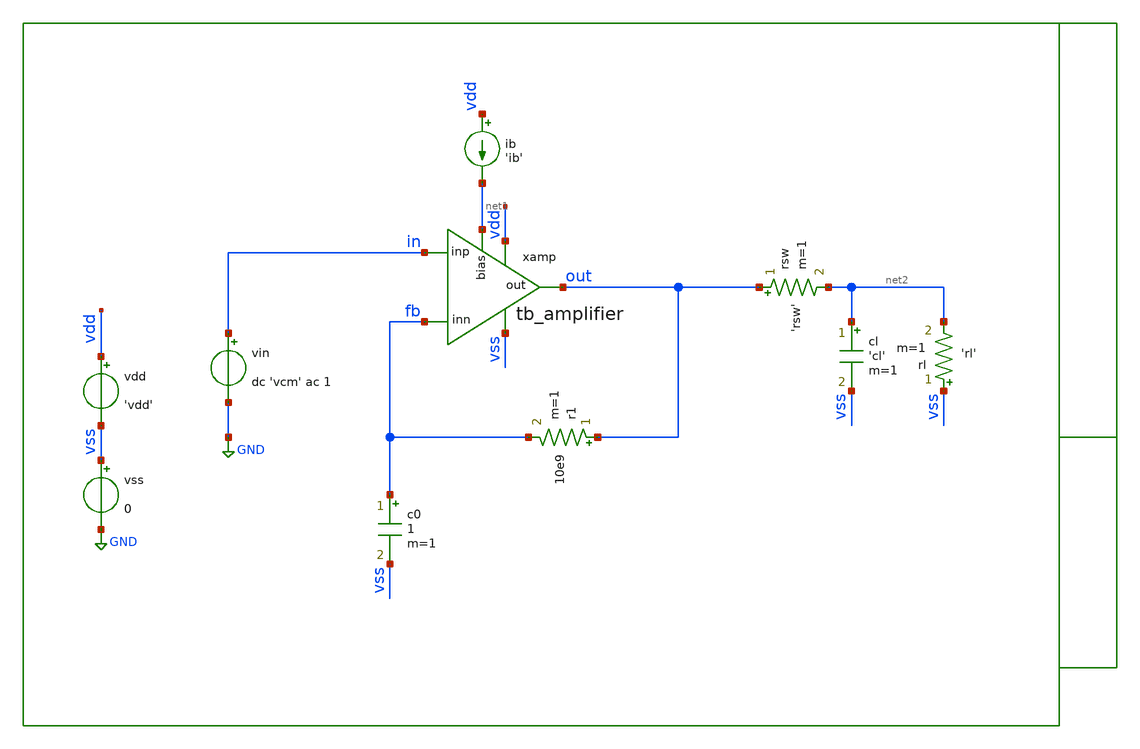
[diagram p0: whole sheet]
** sch_path: xschem/tb/testbuffer/tb_amplifier/no_tb_amplifier.sch
**.subckt no_tb_amplifier
vin in GND dc 'vcm' ac 1
c0 fb vss 1 m=1
r1 out fb 10e9 m=1
ib vdd net1 'ib'
xamp vdd out in fb vss net1 tb_amplifier
vdd vdd vss 'vdd'
vss vss GND 0
cl net2 vss 'cl' m=1
rl vss net2 'rl' m=1
rsw out net2 'rsw' m=1
**** begin user architecture code

* Control

.param vdd=3.3
.param vcm='vdd/2'
.param ib=5u
.param cl=1p
.param rl=10e6
.param rsw=1

.control
save all
noise v(out,vss) vin dec 10 0.1 1e6 1
print inoise_total
print onoise_total
setplot noise1
gnuplot p1 inoise_spectrum
gnuplot p2 onoise_spectrum
set wr_singlescale
set wr_vecnames
wrdata data.csv onoise_spectrum inoise_spectrum
.endc


 * Model Corners

.include $::CORNERS/ngspice/tt.spice
*.include $::CORNERS/ngspice/ff.spice
*.include $::CORNERS/ngspice/ss.spice
*.include $::CORNERS/ngspice/sf.spice
*.include $::CORNERS/ngspice/fs.spice

**** end user architecture code
**.ends

* expanding   symbol:  sch/testbuffer/tb_amplifier/tb_amplifier.sym # of pins=6
** sym_path: xschem/sch/testbuffer/tb_amplifier/tb_amplifier.sym
** sch_path: xschem/sch/testbuffer/tb_amplifier/tb_amplifier.sch
.subckt tb_amplifier vdd out inp inn vss bias
*.ipin inn
*.ipin inp
*.opin out
*.iopin bias
*.iopin vdd
*.iopin vss
XM3 mirr mirr vdd vdd pfet_06v0 L=4u W=16u nf=2 ad='int((nf+1)/2) * W/nf * 0.18u' as='int((nf+2)/2) * W/nf * 0.18u'
+ pd='2*int((nf+1)/2) * (W/nf + 0.18u)' ps='2*int((nf+2)/2) * (W/nf + 0.18u)' nrd='0.18u / W' nrs='0.18u / W'
+ sa=0 sb=0 sd=0 m=2 par=2
XM4 comp mirr vdd vdd pfet_06v0 L=4u W=16u nf=2 ad='int((nf+1)/2) * W/nf * 0.18u' as='int((nf+2)/2) * W/nf * 0.18u'
+ pd='2*int((nf+1)/2) * (W/nf + 0.18u)' ps='2*int((nf+2)/2) * (W/nf + 0.18u)' nrd='0.18u / W' nrs='0.18u / W'
+ sa=0 sb=0 sd=0 m=2 par=2
XM2 comp inp vcm vss nfet_06v0 L=2u W=16u nf=2 ad='int((nf+1)/2) * W/nf * 0.18u' as='int((nf+2)/2) * W/nf * 0.18u'
+ pd='2*int((nf+1)/2) * (W/nf + 0.18u)' ps='2*int((nf+2)/2) * (W/nf + 0.18u)' nrd='0.18u / W' nrs='0.18u / W'
+ sa=0 sb=0 sd=0 m=2 par=2
XM1 mirr inn vcm vss nfet_06v0 L=2u W=16u nf=2 ad='int((nf+1)/2) * W/nf * 0.18u' as='int((nf+2)/2) * W/nf * 0.18u'
+ pd='2*int((nf+1)/2) * (W/nf + 0.18u)' ps='2*int((nf+2)/2) * (W/nf + 0.18u)' nrd='0.18u / W' nrs='0.18u / W'
+ sa=0 sb=0 sd=0 m=2 par=2
XM5 vcm bias vss vss nfet_06v0 L=1u W=16u nf=2 ad='int((nf+1)/2) * W/nf * 0.18u' as='int((nf+2)/2) * W/nf * 0.18u'
+ pd='2*int((nf+1)/2) * (W/nf + 0.18u)' ps='2*int((nf+2)/2) * (W/nf + 0.18u)' nrd='0.18u / W' nrs='0.18u / W'
+ sa=0 sb=0 sd=0 m=2 par=2
XM6 out bias vss vss nfet_06v0 L=1u W=16u nf=2 ad='int((nf+1)/2) * W/nf * 0.18u' as='int((nf+2)/2) * W/nf * 0.18u'
+ pd='2*int((nf+1)/2) * (W/nf + 0.18u)' ps='2*int((nf+2)/2) * (W/nf + 0.18u)' nrd='0.18u / W' nrs='0.18u / W'
+ sa=0 sb=0 sd=0 m=12 par=12
XM7 out comp vdd vdd pfet_06v0 L=1u W=96u nf=12 ad='int((nf+1)/2) * W/nf * 0.18u' as='int((nf+2)/2) * W/nf * 0.18u'
+ pd='2*int((nf+1)/2) * (W/nf + 0.18u)' ps='2*int((nf+2)/2) * (W/nf + 0.18u)' nrd='0.18u / W' nrs='0.18u / W'
+ sa=0 sb=0 sd=0 m=1 par=1
XMB1 bias bias vss vss nfet_06v0 L=1u W=16u nf=2 ad='int((nf+1)/2) * W/nf * 0.18u' as='int((nf+2)/2) * W/nf * 0.18u'
+ pd='2*int((nf+1)/2) * (W/nf + 0.18u)' ps='2*int((nf+2)/2) * (W/nf + 0.18u)' nrd='0.18u / W' nrs='0.18u / W'
+ sa=0 sb=0 sd=0 m=2 par=2
XMB2 vbm bias vss vss nfet_06v0 L=1u W=16u nf=2 ad='int((nf+1)/2) * W/nf * 0.18u' as='int((nf+2)/2) * W/nf * 0.18u'
+ pd='2*int((nf+1)/2) * (W/nf + 0.18u)' ps='2*int((nf+2)/2) * (W/nf + 0.18u)' nrd='0.18u / W' nrs='0.18u / W'
+ sa=0 sb=0 sd=0 m=2 par=2
XMB3 vbm vbm vbt vdd pfet_06v0 L=1u W=16u nf=2 ad='int((nf+1)/2) * W/nf * 0.18u' as='int((nf+2)/2) * W/nf * 0.18u'
+ pd='2*int((nf+1)/2) * (W/nf + 0.18u)' ps='2*int((nf+2)/2) * (W/nf + 0.18u)' nrd='0.18u / W' nrs='0.18u / W'
+ sa=0 sb=0 sd=0 m=1 par=1
XMB4 vbt vbt vdd vdd pfet_06v0 L=1u W=16u nf=2 ad='int((nf+1)/2) * W/nf * 0.18u' as='int((nf+2)/2) * W/nf * 0.18u'
+ pd='2*int((nf+1)/2) * (W/nf + 0.18u)' ps='2*int((nf+2)/2) * (W/nf + 0.18u)' nrd='0.18u / W' nrs='0.18u / W'
+ sa=0 sb=0 sd=0 m=1 par=1
XRCC gc comp vdd ppolyf_u_1k_6p0 r_width=2e-6 r_length=38e-6 s=1 m=1
XMDUM1 vss vss vss vss nfet_06v0 L=2u W=16u nf=2 ad='int((nf+1)/2) * W/nf * 0.18u' as='int((nf+2)/2) * W/nf * 0.18u'
+ pd='2*int((nf+1)/2) * (W/nf + 0.18u)' ps='2*int((nf+2)/2) * (W/nf + 0.18u)' nrd='0.18u / W' nrs='0.18u / W'
+ sa=0 sb=0 sd=0 m=2 par=2
XMDUM2 vdd vdd vdd vdd pfet_06v0 L=4u W=16u nf=2 ad='int((nf+1)/2) * W/nf * 0.18u' as='int((nf+2)/2) * W/nf * 0.18u'
+ pd='2*int((nf+1)/2) * (W/nf + 0.18u)' ps='2*int((nf+2)/2) * (W/nf + 0.18u)' nrd='0.18u / W' nrs='0.18u / W'
+ sa=0 sb=0 sd=0 m=4 par=4
XC1 out gc cap_mim_2f0_m4m5_noshield c_width=30e-6 c_length=30e-6 m=1
.ends

.GLOBAL GND
.end
